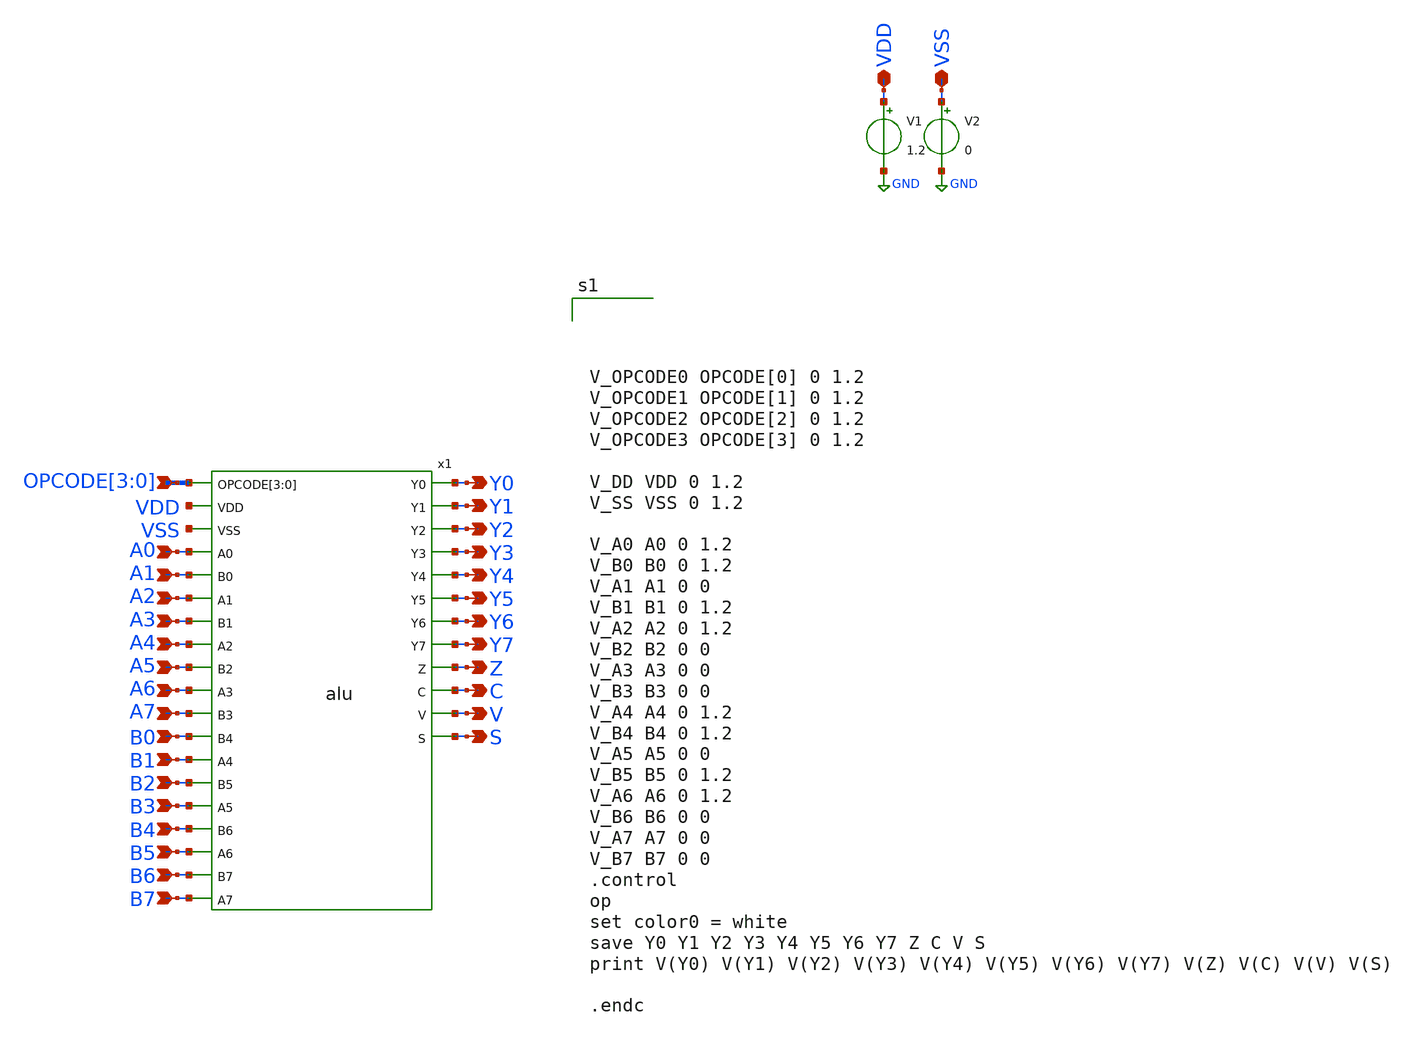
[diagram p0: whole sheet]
** sch_path: design/xschem/TEST_BENCHES/ALU_TB.sch
**.subckt ALU_TB VDD VSS A7 A6 A5 A4 A3 A2 A1 A0 B1 B2 B3 B0 B6 B7 B5 B4 Y0 Y1 Y2 Y3 Y4 Y5 Y6 Y7 Z C
*+ V S OPCODE[3],OPCODE[2],OPCODE[1],OPCODE[0]
*.iopin VDD
*.iopin VSS
*.ipin A7
*.ipin A6
*.ipin A5
*.ipin A4
*.ipin A3
*.ipin A2
*.ipin A1
*.ipin A0
*.ipin B1
*.ipin B2
*.ipin B3
*.ipin B0
*.ipin B6
*.ipin B7
*.ipin B5
*.ipin B4
*.opin Y0
*.opin Y1
*.opin Y2
*.opin Y3
*.opin Y4
*.opin Y5
*.opin Y6
*.opin Y7
*.opin Z
*.opin C
*.opin V
*.opin S
*.ipin OPCODE[3],OPCODE[2],OPCODE[1],OPCODE[0]
V1 VDD GND 1.2
V2 VSS GND 0
x1 OPCODE[3] OPCODE[2] OPCODE[1] OPCODE[0] A0 A1 Y0 Z VDD VSS A2 C A3 Y1 A4 V A5 Y2 S A6 Y3 A7 B0 Y4
+ B1 B2 B3 Y5 B4 Y6 B5 B6 Y7 B7 VSS VDD alu
**** begin user architecture code

** opencircuitdesign pdks install
.lib $::SKYWATER_MODELS/sky130.lib.spice tt_mm






V_OPCODE0 OPCODE[0] 0 1.2
V_OPCODE1 OPCODE[1] 0 1.2
V_OPCODE2 OPCODE[2] 0 1.2
V_OPCODE3 OPCODE[3] 0 1.2

V_DD VDD 0 1.2
V_SS VSS 0 1.2

V_A0 A0 0 1.2
V_B0 B0 0 1.2
V_A1 A1 0 0
V_B1 B1 0 1.2
V_A2 A2 0 1.2
V_B2 B2 0 0
V_A3 A3 0 0
V_B3 B3 0 0
V_A4 A4 0 1.2
V_B4 B4 0 1.2
V_A5 A5 0 0
V_B5 B5 0 1.2
V_A6 A6 0 1.2
V_B6 B6 0 0
V_A7 A7 0 0
V_B7 B7 0 0
.control
op
set color0 = white
save Y0 Y1 Y2 Y3 Y4 Y5 Y6 Y7 Z C V S
print V(Y0) V(Y1) V(Y2) V(Y3) V(Y4) V(Y5) V(Y6) V(Y7) V(Z) V(C) V(V) V(S)

.endc


**** end user architecture code
**.ends
.GLOBAL GND
.end
